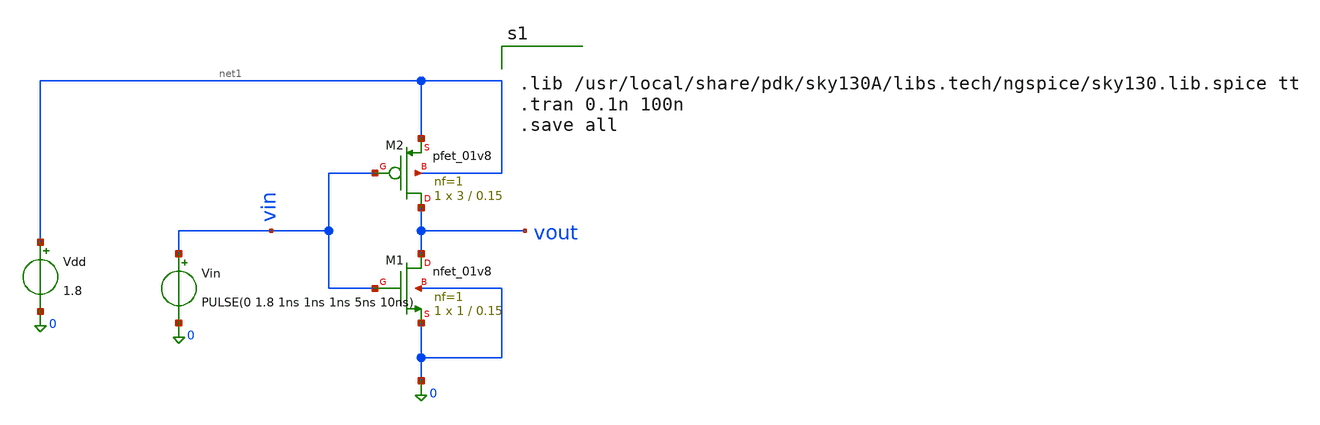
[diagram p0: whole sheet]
** sch_path: assignment_tran.sch
**.subckt assignment_tran
Vin vin 0 PULSE(0 1.8 1ns 1ns 1ns 5ns 10ns)
Vdd net1 0 1.8
XM2 vout vin net1 net1 sky130_fd_pr__pfet_01v8 L=0.15 W=3 nf=1 ad='int((1 + 1)/2) * 3 / 1 * 0.29' as='int((1 + 2)/2) * 3 / 1 * 0.29'
+ pd='2*int((1 + 1)/2) * (3 / 1 + 0.29)' ps='2*int((1 + 2)/2) * (3 / 1 + 0.29)' nrd='0.29 / 3 ' nrs='0.29 / 3 '
+ sa=0 sb=0 sd=0 mult=1 m=1
XM1 vout vin 0 0 sky130_fd_pr__nfet_01v8 L=0.15 W=1 nf=1 ad='int((1 + 1)/2) * 1 / 1 * 0.29' as='int((1 + 2)/2) * 1 / 1 * 0.29'
+ pd='2*int((1 + 1)/2) * (1 / 1 + 0.29)' ps='2*int((1 + 2)/2) * (1 / 1 + 0.29)' nrd='0.29 / 1 ' nrs='0.29 / 1 '
+ sa=0 sb=0 sd=0 mult=1 m=1
**** begin user architecture code


.lib /usr/local/share/pdk/sky130A/libs.tech/ngspice/sky130.lib.spice tt
.tran 0.1n 100n
.save all




**** end user architecture code
**.ends
.end
